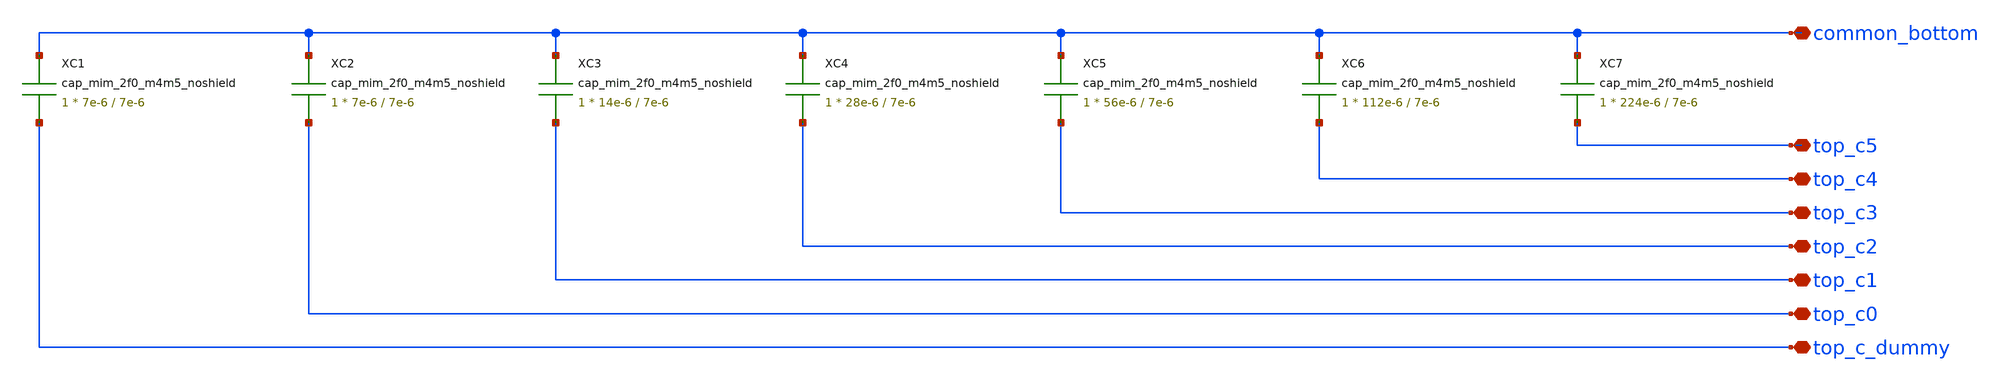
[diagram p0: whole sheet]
** sch_path: cdac/mim_cap_array_8x8/rev000.obsolete/mim_cap_array8x8_15step.sch
**.subckt mim_cap_array8x8_15step common_bottom top_c5 top_c4 top_c3 top_c2 top_c1 top_c0
*+ top_c_dummy
*.iopin common_bottom
*.iopin top_c5
*.iopin top_c4
*.iopin top_c3
*.iopin top_c2
*.iopin top_c1
*.iopin top_c0
*.iopin top_c_dummy
XC1 common_bottom top_c_dummy cap_mim_2f0_m4m5_noshield c_width=7e-6 c_length=7e-6 m=1
XC2 common_bottom top_c0 cap_mim_2f0_m4m5_noshield c_width=7e-6 c_length=7e-6 m=1
XC3 common_bottom top_c1 cap_mim_2f0_m4m5_noshield c_width=14e-6 c_length=7e-6 m=1
XC4 common_bottom top_c2 cap_mim_2f0_m4m5_noshield c_width=28e-6 c_length=7e-6 m=1
XC5 common_bottom top_c3 cap_mim_2f0_m4m5_noshield c_width=56e-6 c_length=7e-6 m=1
XC6 common_bottom top_c4 cap_mim_2f0_m4m5_noshield c_width=112e-6 c_length=7e-6 m=1
XC7 common_bottom top_c5 cap_mim_2f0_m4m5_noshield c_width=224e-6 c_length=7e-6 m=1
**.ends
.end
